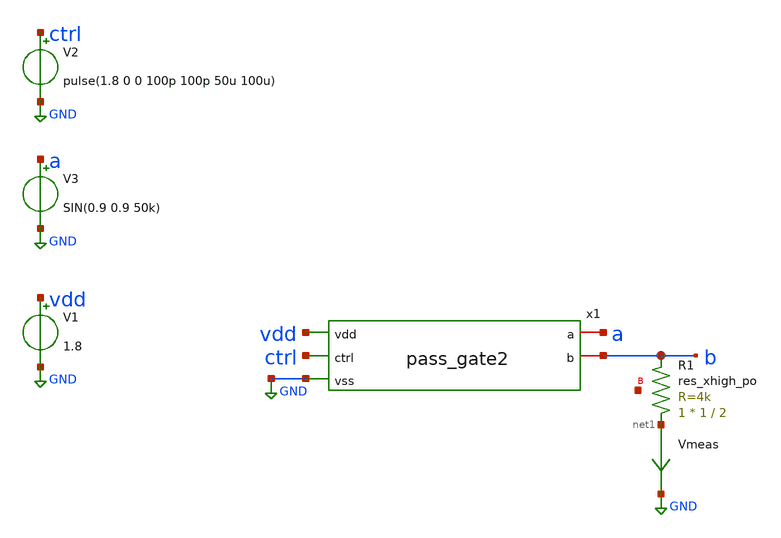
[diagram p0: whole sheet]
** sch_path: custom_gds/tt_um_tim2305_adc_dac/xschem/pass_gate2_tb.sch
**.subckt pass_gate2_tb
V1 vdd GND 1.8
V3 a GND SIN(0.9 0.9 50k)
V2 ctrl GND pulse(1.8 0 0 100p 100p 50u 100u)
XR1 net1 b net2 sky130_fd_pr__res_xhigh_po W=1 L=2 mult=1 m=1
Vmeas net1 GND 0
.save i(vmeas)
x1 vdd ctrl a b GND pass_gate2
**** begin user architecture code


.tran 100n 100u
.save all
.lib /home/ttuser/pdk/sky130A/libs.tech/ngspice/sky130.lib.spice tt


**** end user architecture code
**.ends
.GLOBAL GND
.end
